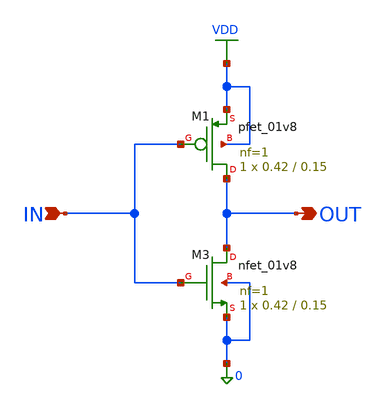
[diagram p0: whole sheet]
** sch_path: designs_backup/designs/inv_mixed/xschem/inv.sch
**.subckt inv OUT IN
*.opin OUT
*.ipin IN
XM1 OUT IN VDD VDD sky130_fd_pr__pfet_01v8 L=0.15 W=0.42 nf=1 ad='int((1 + 1)/2) * 0.42 / 1 * 0.29' as='int((1 + 2)/2) * 0.42 / 1 * 0.29'
+ pd='2*int((1 + 1)/2) * (0.42 / 1 + 0.29)' ps='2*int((1 + 2)/2) * (0.42 / 1 + 0.29)' nrd='0.29 / 0.42 '
+ nrs='0.29 / 0.42 ' sa=0 sb=0 sd=0 mult=1 m=1
XM3 OUT IN 0 0 sky130_fd_pr__nfet_01v8 L=0.15 W=0.42 nf=1 ad='int((1 + 1)/2) * 0.42 / 1 * 0.29' as='int((1 + 2)/2) * 0.42 / 1 * 0.29'
+ pd='2*int((1 + 1)/2) * (0.42 / 1 + 0.29)' ps='2*int((1 + 2)/2) * (0.42 / 1 + 0.29)' nrd='0.29 / 0.42 '
+ nrs='0.29 / 0.42 ' sa=0 sb=0 sd=0 mult=1 m=1
**.ends
.GLOBAL VDD
.end
